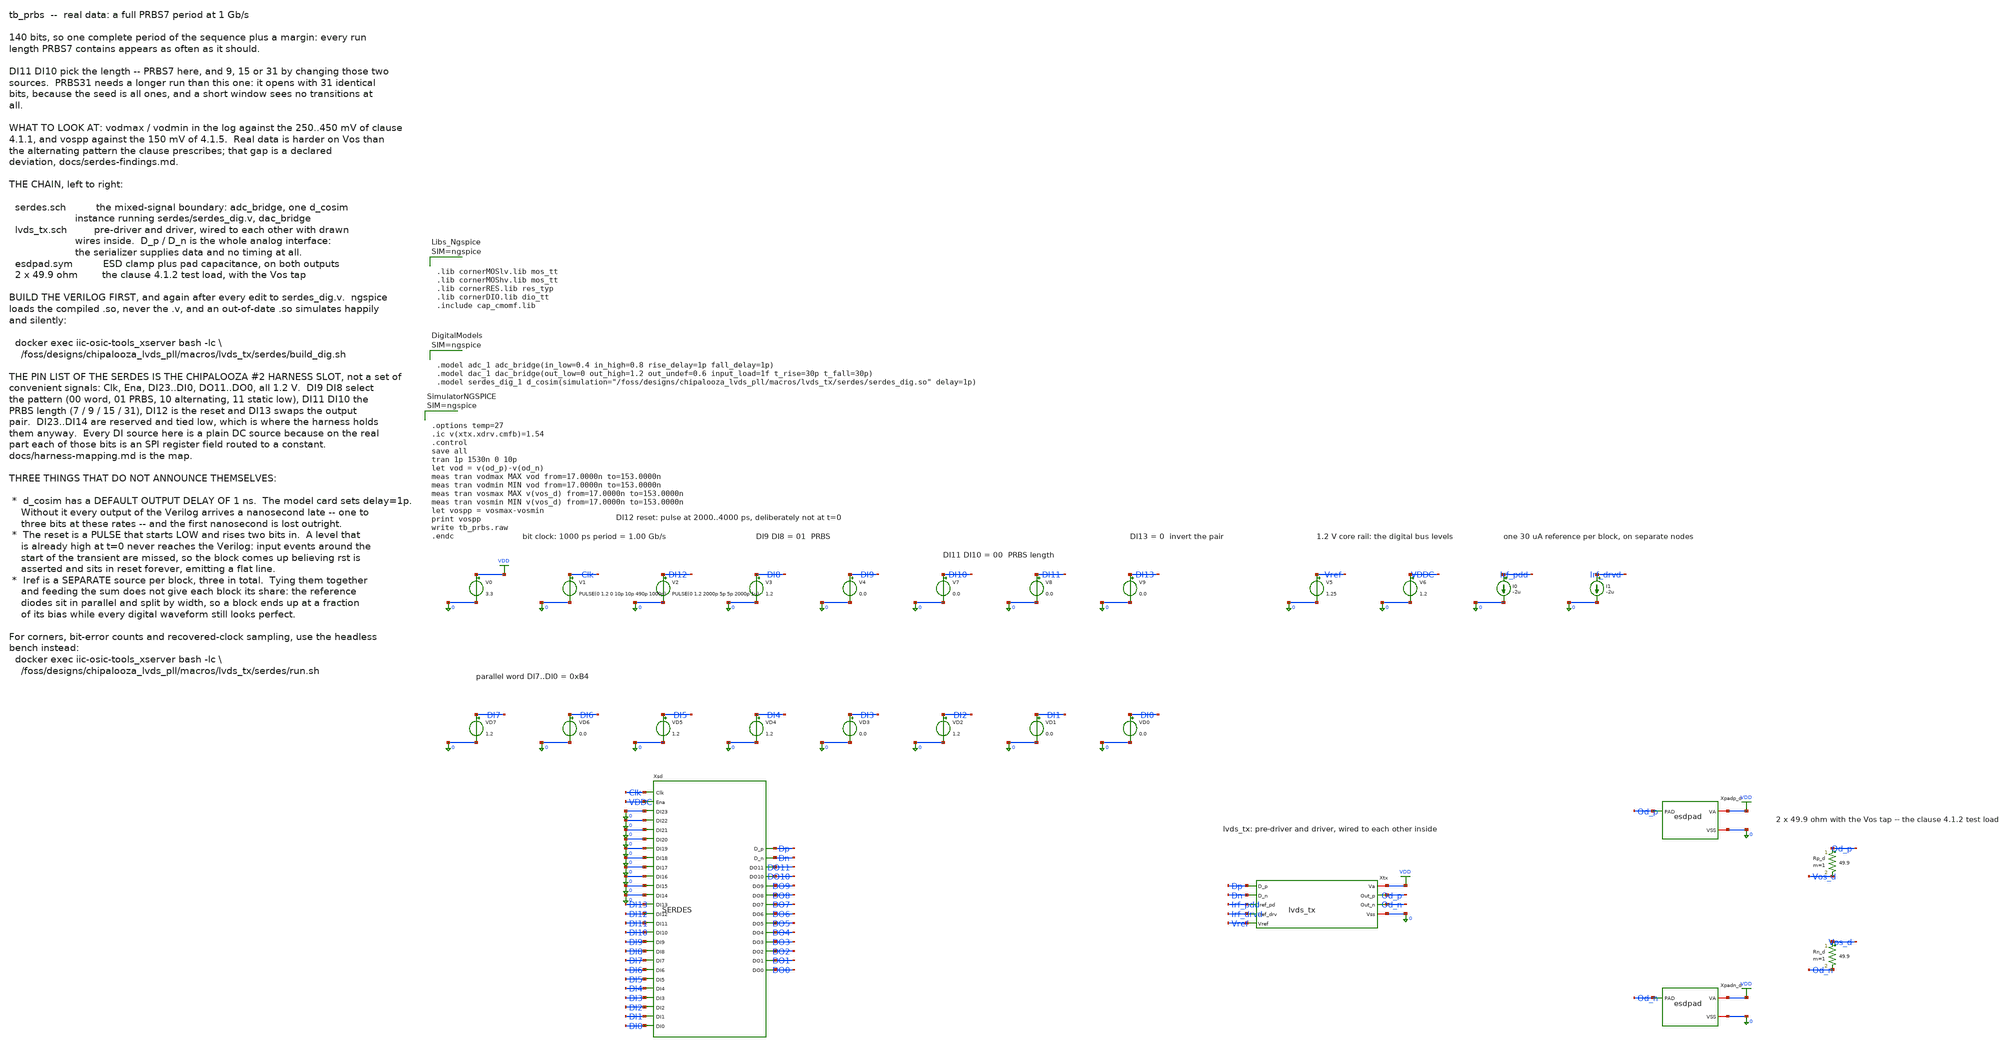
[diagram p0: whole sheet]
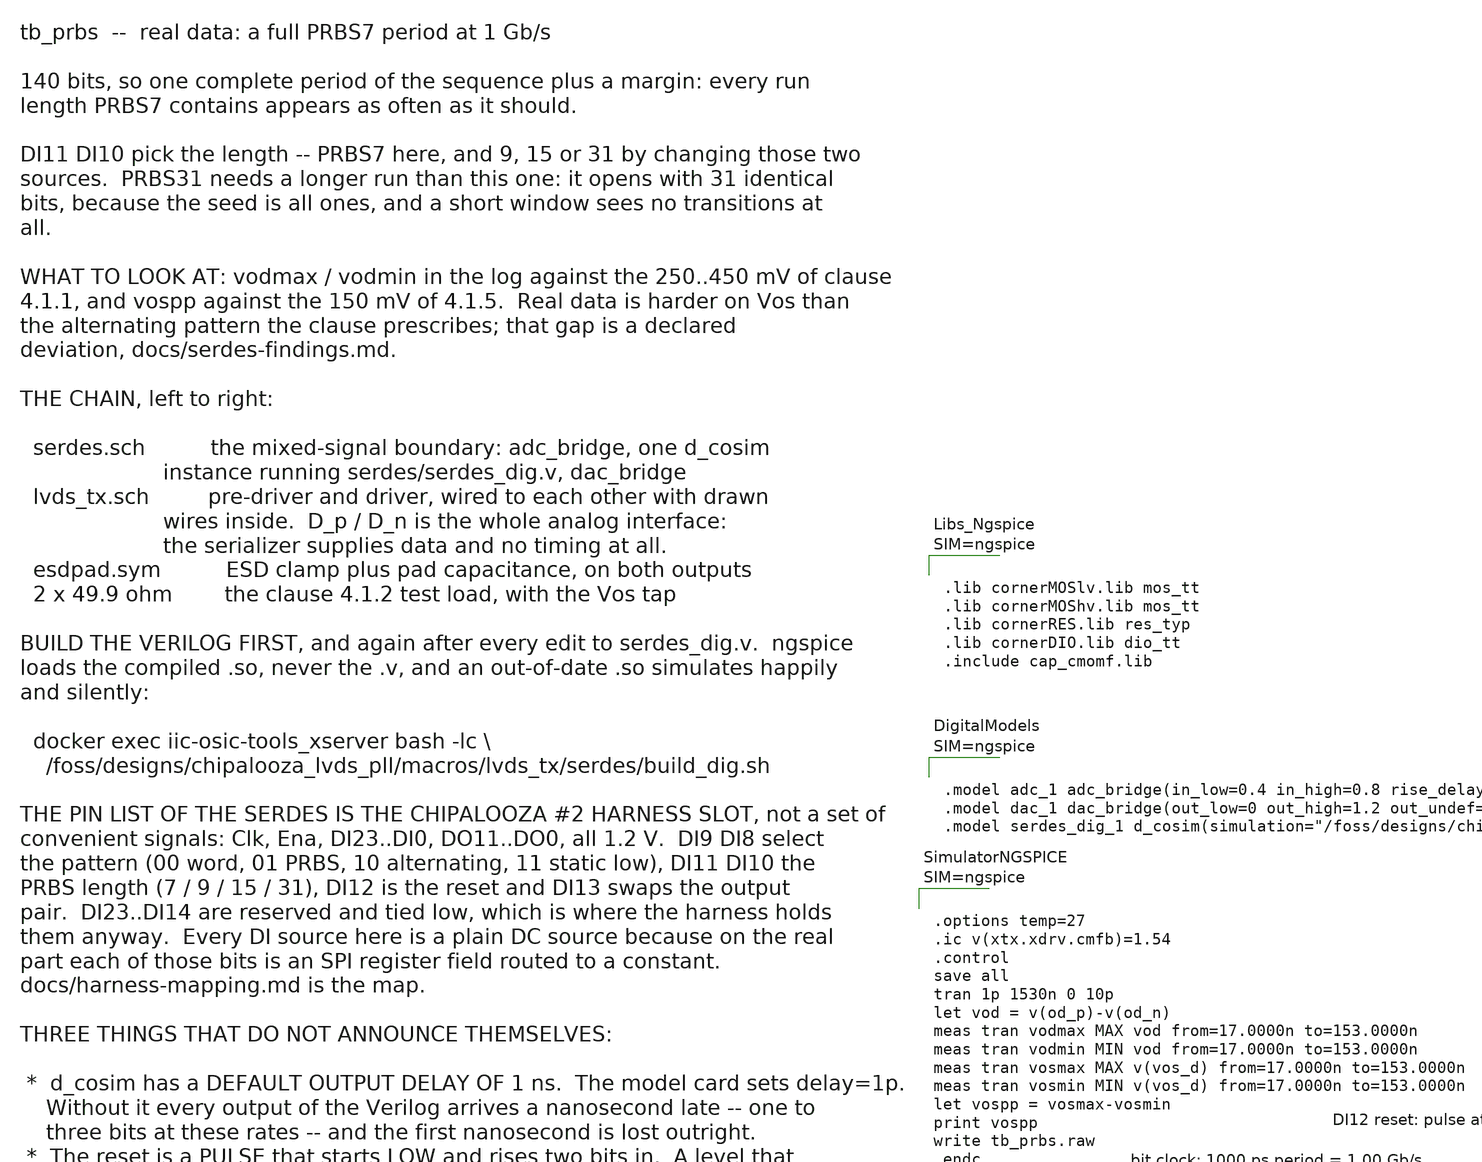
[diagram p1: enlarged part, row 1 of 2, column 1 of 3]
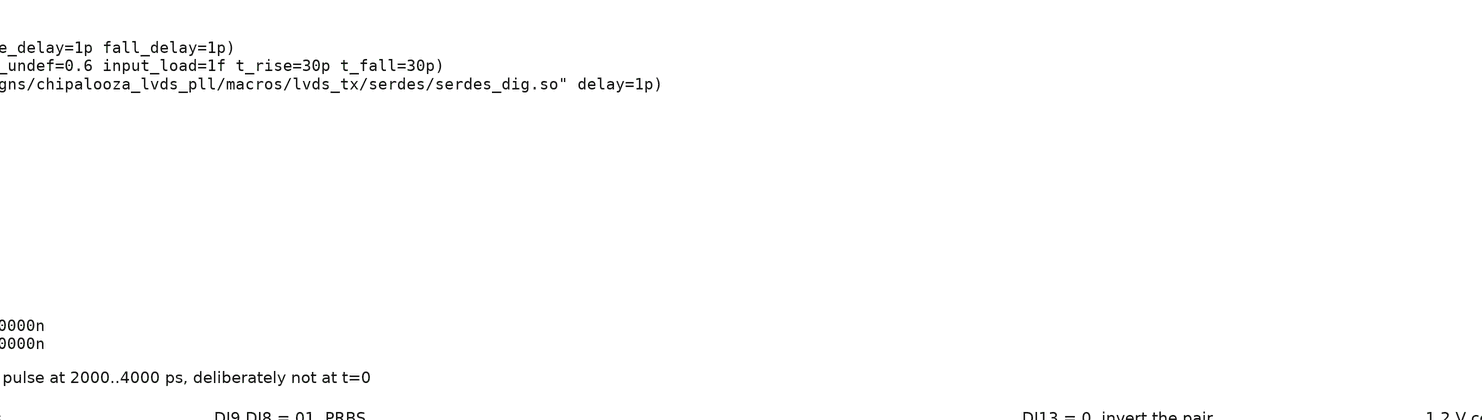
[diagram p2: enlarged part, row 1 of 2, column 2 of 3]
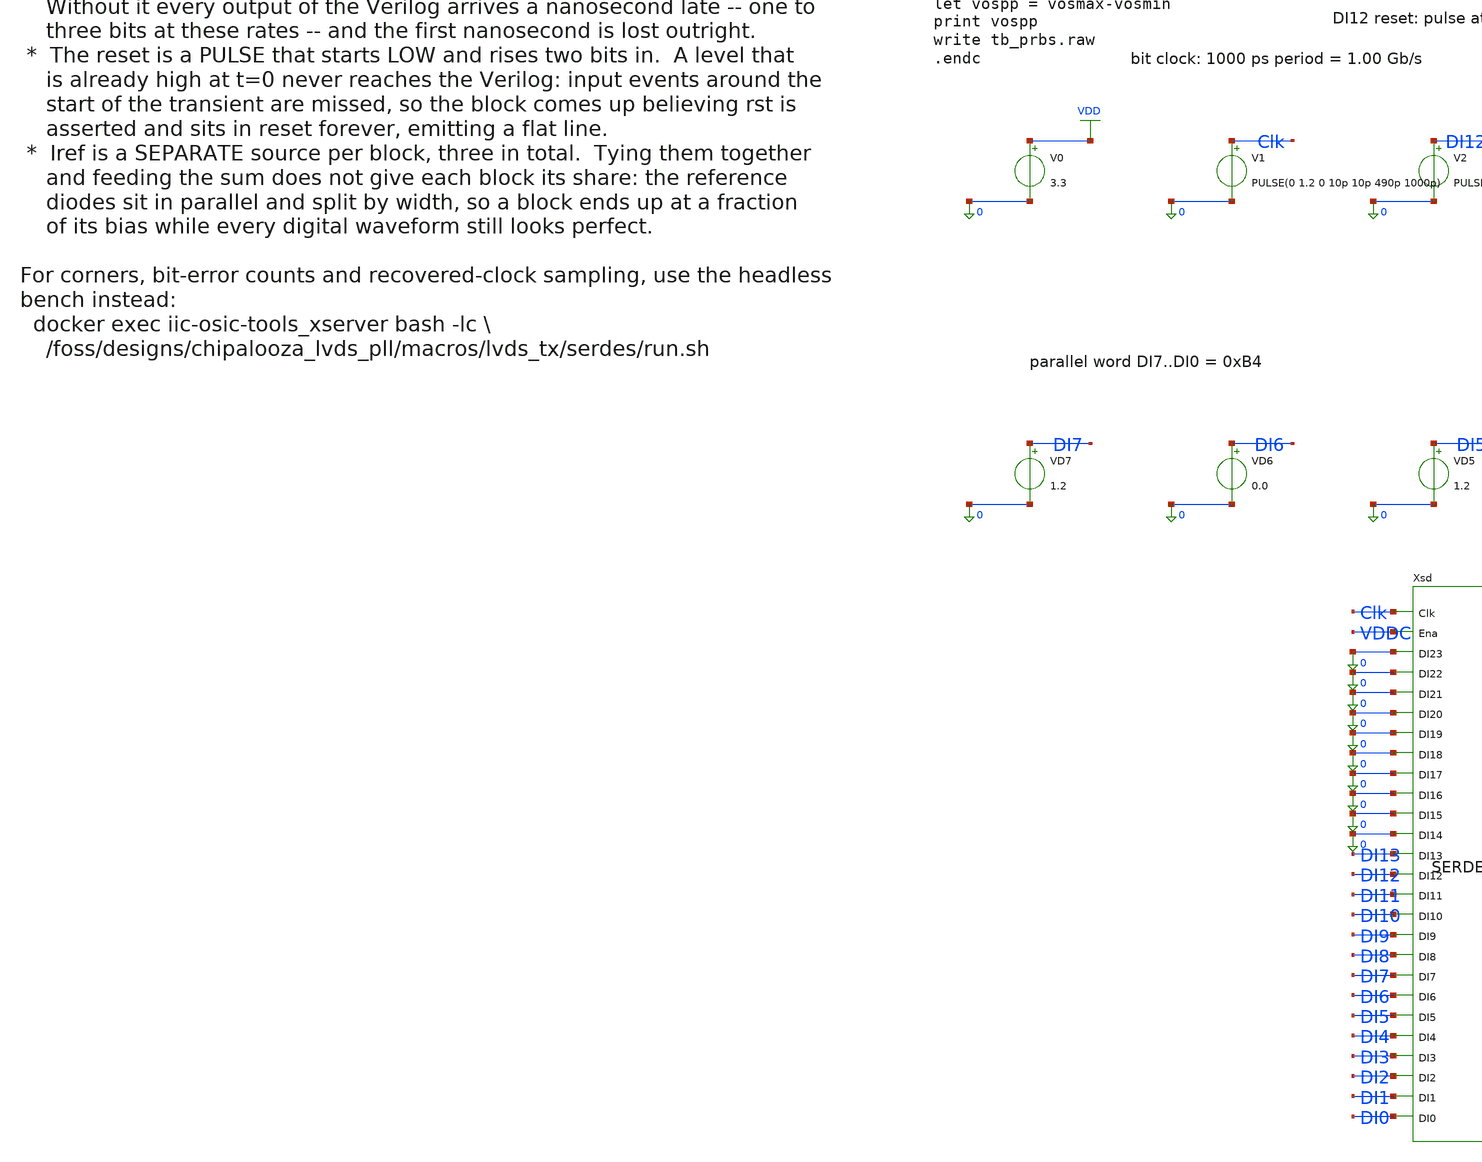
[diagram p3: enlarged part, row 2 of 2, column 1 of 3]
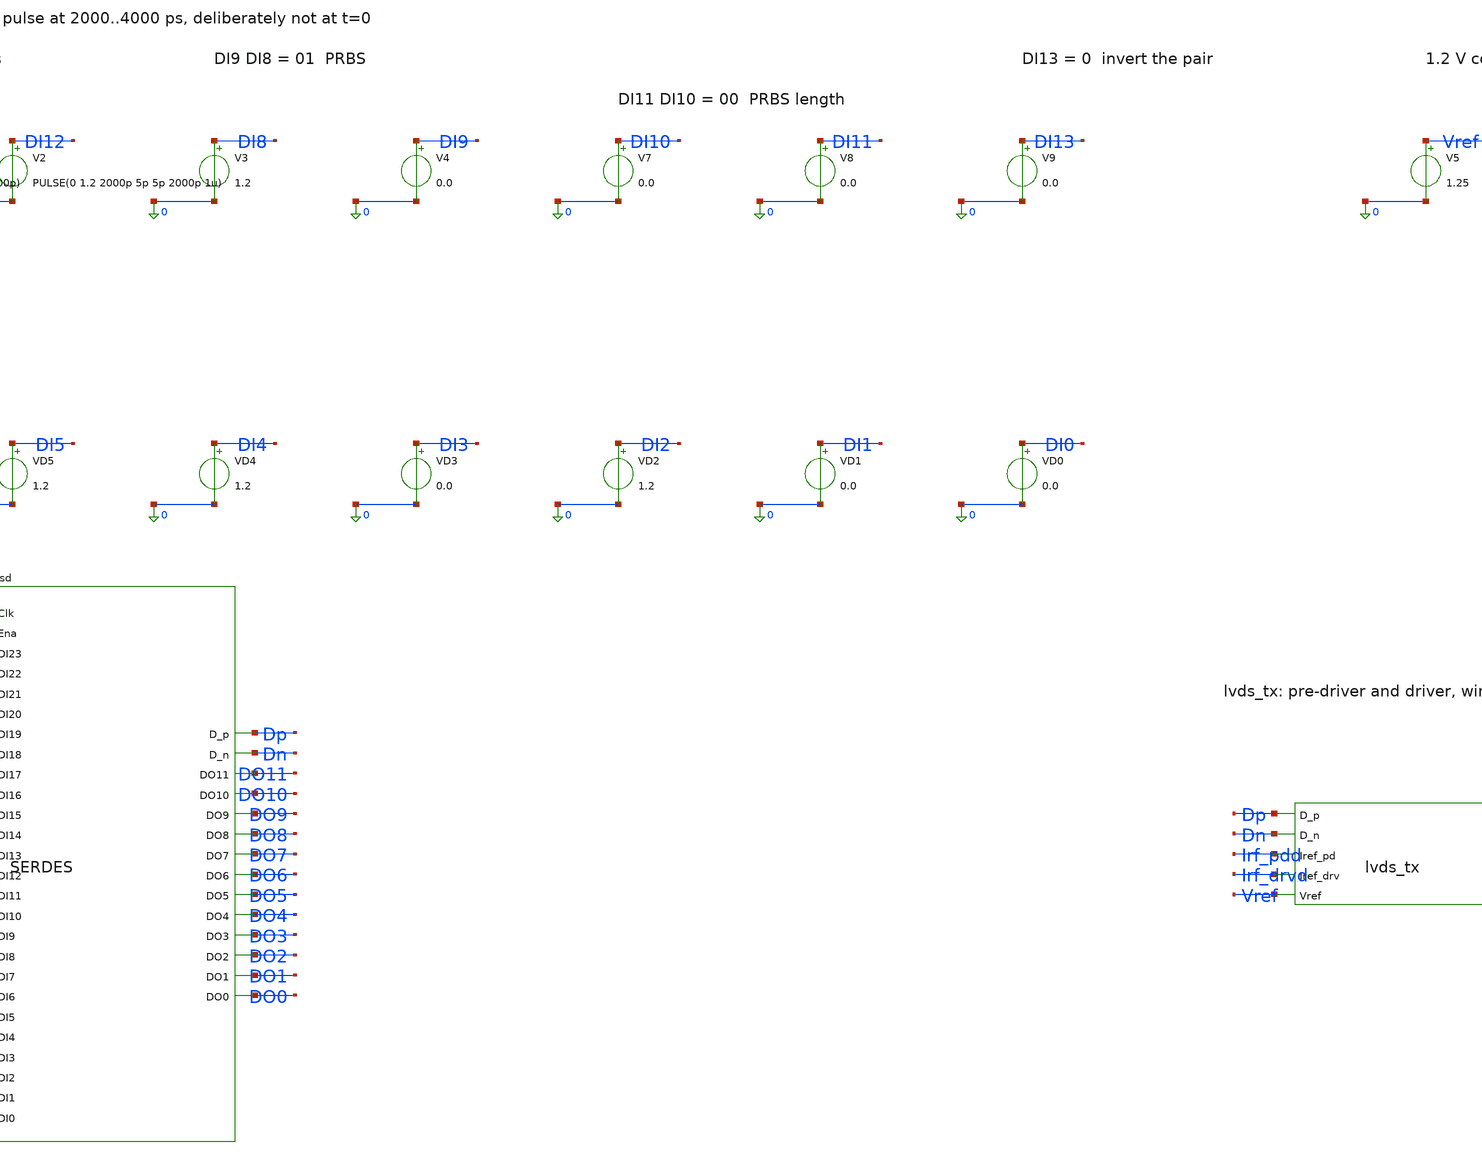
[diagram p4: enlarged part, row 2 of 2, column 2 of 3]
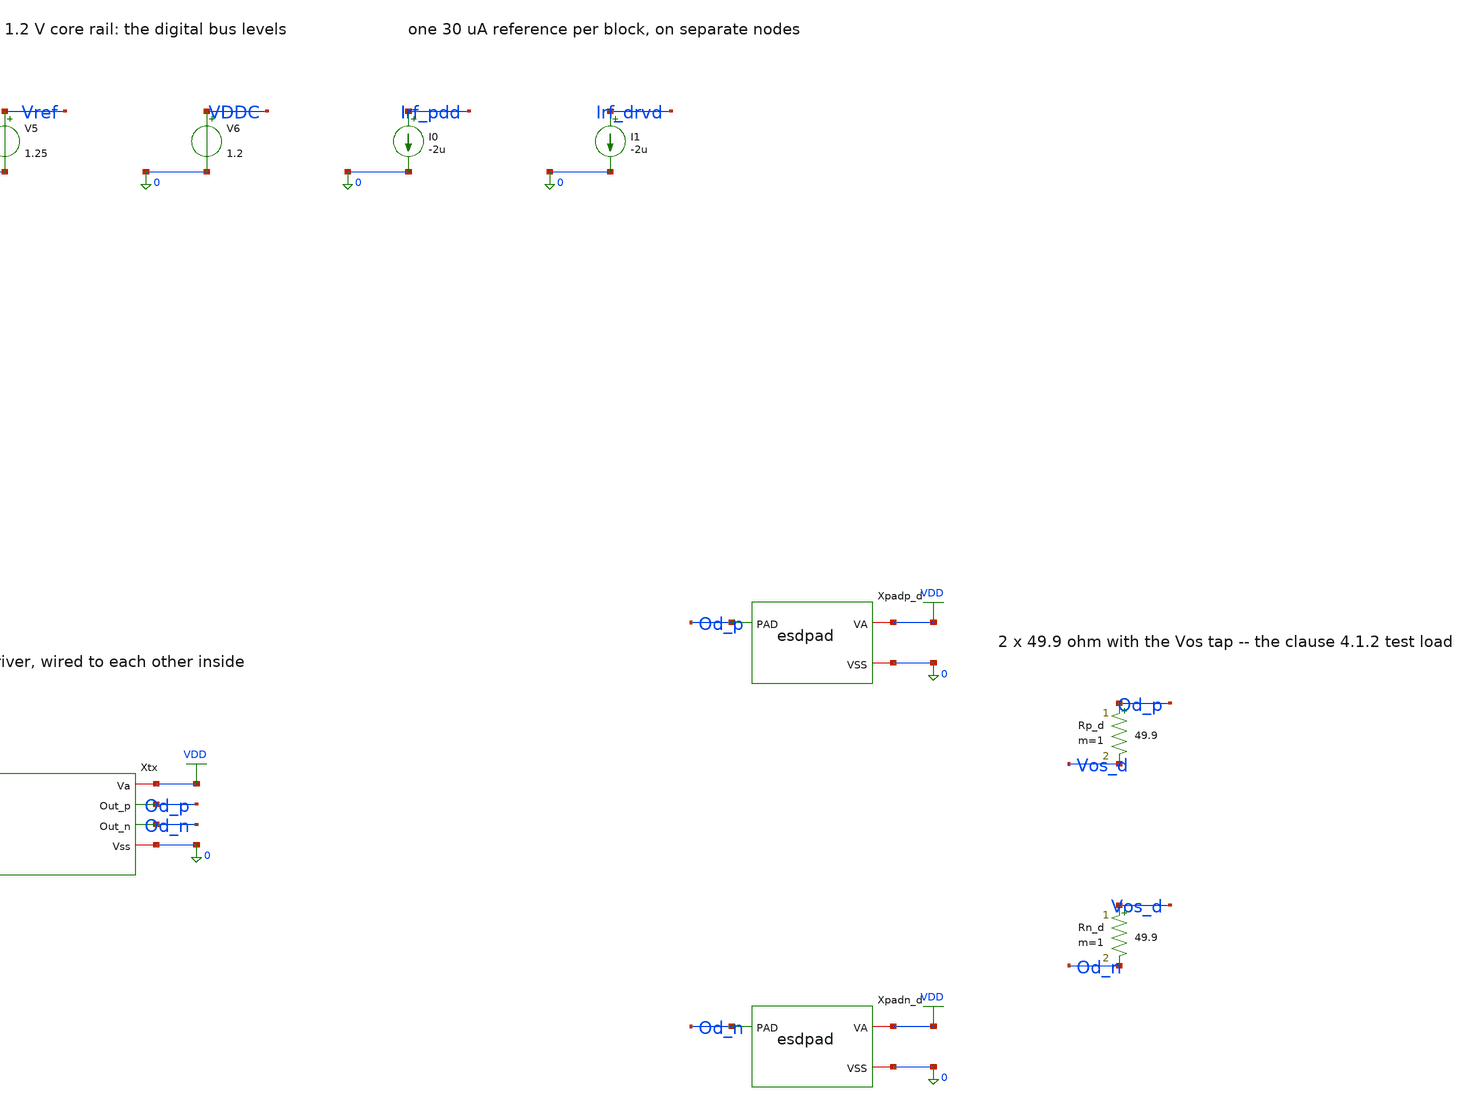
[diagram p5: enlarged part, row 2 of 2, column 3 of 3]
** sch_path: macros/lvds_tx/testbenches/xschem/tb_prbs.sch
**.subckt tb_prbs
V0 VDD 0 3.3
V1 Clk 0 PULSE(0 1.2 0 10p 10p 490p 1000p)
V2 DI12 0 PULSE(0 1.2 2000p 5p 5p 2000p 1u)
V3 DI8 0 1.2
V4 DI9 0 0.0
V7 DI10 0 0.0
V8 DI11 0 0.0
V9 DI13 0 0.0
VD7 DI7 0 1.2
VD6 DI6 0 0.0
VD5 DI5 0 1.2
VD4 DI4 0 1.2
VD3 DI3 0 0.0
VD2 DI2 0 1.2
VD1 DI1 0 0.0
VD0 DI0 0 0.0
V5 Vref 0 1.25
V6 VDDC 0 1.2
I0 Irf_pdd 0 -2u
I1 Irf_drvd 0 -2u
Xsd Clk VDDC 0 0 0 0 0 0 0 0 0 0 DI13 DI12 DI11 DI10 DI9 DI8 DI7 DI6 DI5 DI4 DI3 DI2 DI1 DI0 Dp Dn
+ DO11 DO10 DO9 DO8 DO7 DO6 DO5 DO4 DO3 DO2 DO1 DO0 serdes
Xtx Dp Dn Irf_pdd Irf_drvd Vref VDD Od_p Od_n 0 lvds_tx
Xpadp_d Od_p VDD 0 esdpad
Xpadn_d Od_n VDD 0 esdpad
Rp_d Od_p Vos_d 49.9 m=1
Rn_d Vos_d Od_n 49.9 m=1
**** begin user architecture code



.lib cornerMOSlv.lib mos_tt
.lib cornerMOShv.lib mos_tt
.lib cornerRES.lib res_typ
.lib cornerDIO.lib dio_tt
.include cap_cmomf.lib






.model adc_1 adc_bridge(in_low=0.4 in_high=0.8 rise_delay=1p fall_delay=1p)
.model dac_1 dac_bridge(out_low=0 out_high=1.2 out_undef=0.6 input_load=1f t_rise=30p t_fall=30p)
.model serdes_dig_1
+ d_cosim(simulation="/foss/designs/chipalooza_lvds_pll/macros/lvds_tx/serdes/serdes_dig.so" delay=1p)






.options temp=27
.ic v(xtx.xdrv.cmfb)=1.54
.control
save all
tran 1p 1530n 0 10p
let vod = v(od_p)-v(od_n)
meas tran vodmax MAX vod from=17.0000n to=153.0000n
meas tran vodmin MIN vod from=17.0000n to=153.0000n
meas tran vosmax MAX v(vos_d) from=17.0000n to=153.0000n
meas tran vosmin MIN v(vos_d) from=17.0000n to=153.0000n
let vospp = vosmax-vosmin
print vospp
write tb_prbs.raw
.endc



**** end user architecture code
**.ends

* expanding   symbol:  serdes.sym # of pins=40
** sym_path: macros/lvds_tx/schematic/xschem/serdes.sym
** sch_path: macros/lvds_tx/schematic/xschem/serdes.sch
.subckt serdes Clk Ena DI23 DI22 DI21 DI20 DI19 DI18 DI17 DI16 DI15 DI14 DI13 DI12 DI11 DI10 DI9 DI8
+ DI7 DI6 DI5 DI4 DI3 DI2 DI1 DI0 D_p D_n DO11 DO10 DO9 DO8 DO7 DO6 DO5 DO4 DO3 DO2 DO1 DO0
*.ipin Clk
*.ipin Ena
*.ipin DI23
*.ipin DI22
*.ipin DI21
*.ipin DI20
*.ipin DI19
*.ipin DI18
*.ipin DI17
*.ipin DI16
*.ipin DI15
*.ipin DI14
*.ipin DI13
*.ipin DI12
*.ipin DI11
*.ipin DI10
*.ipin DI9
*.ipin DI8
*.ipin DI7
*.ipin DI6
*.ipin DI5
*.ipin DI4
*.ipin DI3
*.ipin DI2
*.ipin DI1
*.ipin DI0
*.opin D_p
*.opin D_n
*.opin DO11
*.opin DO10
*.opin DO9
*.opin DO8
*.opin DO7
*.opin DO6
*.opin DO5
*.opin DO4
*.opin DO3
*.opin DO2
*.opin DO1
*.opin DO0
A100 [ Clk ] [ dclk ] adc_1
A101 [ Ena ] [ dena ] adc_1
A102 [ DI23 ] [ ddi23 ] adc_1
A103 [ DI22 ] [ ddi22 ] adc_1
A104 [ DI21 ] [ ddi21 ] adc_1
A105 [ DI20 ] [ ddi20 ] adc_1
A106 [ DI19 ] [ ddi19 ] adc_1
A107 [ DI18 ] [ ddi18 ] adc_1
A108 [ DI17 ] [ ddi17 ] adc_1
A109 [ DI16 ] [ ddi16 ] adc_1
A110 [ DI15 ] [ ddi15 ] adc_1
A111 [ DI14 ] [ ddi14 ] adc_1
A112 [ DI13 ] [ ddi13 ] adc_1
A113 [ DI12 ] [ ddi12 ] adc_1
A114 [ DI11 ] [ ddi11 ] adc_1
A115 [ DI10 ] [ ddi10 ] adc_1
A116 [ DI9 ] [ ddi9 ] adc_1
A117 [ DI8 ] [ ddi8 ] adc_1
A118 [ DI7 ] [ ddi7 ] adc_1
A119 [ DI6 ] [ ddi6 ] adc_1
A120 [ DI5 ] [ ddi5 ] adc_1
A121 [ DI4 ] [ ddi4 ] adc_1
A122 [ DI3 ] [ ddi3 ] adc_1
A123 [ DI2 ] [ ddi2 ] adc_1
A124 [ DI1 ] [ ddi1 ] adc_1
A125 [ DI0 ] [ ddi0 ] adc_1
Adig [ dclk dena ddi23 ddi22 ddi21 ddi20 ddi19 ddi18 ddi17 ddi16 ddi15 ddi14 ddi13 ddi12 ddi11 ddi10
+ ddi9 ddi8 ddi7 ddi6 ddi5 ddi4 ddi3 ddi2 ddi1 ddi0 ] [ ddp ddn ddo11 ddo10 ddo9 ddo8 ddo7 ddo6 ddo5 ddo4
+ ddo3 ddo2 ddo1 ddo0 ] serdes_dig_1
A200 [ ddp ] [ D_p ] dac_1
A201 [ ddn ] [ D_n ] dac_1
A202 [ ddo11 ] [ DO11 ] dac_1
A203 [ ddo10 ] [ DO10 ] dac_1
A204 [ ddo9 ] [ DO9 ] dac_1
A205 [ ddo8 ] [ DO8 ] dac_1
A206 [ ddo7 ] [ DO7 ] dac_1
A207 [ ddo6 ] [ DO6 ] dac_1
A208 [ ddo5 ] [ DO5 ] dac_1
A209 [ ddo4 ] [ DO4 ] dac_1
A210 [ ddo3 ] [ DO3 ] dac_1
A211 [ ddo2 ] [ DO2 ] dac_1
A212 [ ddo1 ] [ DO1 ] dac_1
A213 [ ddo0 ] [ DO0 ] dac_1
.ends


* expanding   symbol:  lvds_tx.sym # of pins=9
** sym_path: macros/lvds_tx/schematic/xschem/lvds_tx.sym
** sch_path: macros/lvds_tx/schematic/xschem/lvds_tx.sch
.subckt lvds_tx D_p D_n Iref_pd Iref_drv Vref Va Out_p Out_n Vss
*.ipin D_p
*.ipin D_n
*.ipin Iref_pd
*.ipin Iref_drv
*.ipin Vref
*.iopin Va
*.iopin Vss
*.opin Out_p
*.opin Out_n
Xm_pd Iref_pd Iref_pd_30u Va Vss iref_x15
Xm_drv Iref_drv Iref_drv_30u Va Vss iref_x15
Xpd D_p D_n Iref_pd_30u In_p In_n Va Vss predriver
Xdrv Va Out_p In_p In_n Iref_drv_30u Vref Out_n Vss Driver
.ends


* expanding   symbol:  esdpad.sym # of pins=3
** sym_path: macros/lvds_tx/schematic/xschem/esdpad.sym
** sch_path: macros/lvds_tx/schematic/xschem/esdpad.sch
.subckt esdpad PAD VA VSS
*.iopin PAD
*.iopin VA
*.iopin VSS
XDdvdd VA PAD VSS diodevdd_4kv m=1
XDdvss VA PAD VSS diodevss_4kv m=1
Cpad PAD VSS 90f m=1
.ends


* expanding   symbol:  iref_x15.sym # of pins=4
** sym_path: macros/iref_x15/schematic/xschem/iref_x15.sym
** sch_path: macros/iref_x15/schematic/xschem/iref_x15.sch
.subckt iref_x15 IREF_IN IREF_OUT Va Vss
*.ipin IREF_IN
*.opin IREF_OUT
*.iopin Va
*.iopin Vss
XMn1 IREF_IN IREF_IN Vss Vss sg13_hv_nmos w=3.2u l=2u ng=1 m=1 mm_ok=1
XMn2 CASC IREF_IN Vss Vss sg13_hv_nmos w=48u l=2u ng=6 m=1 mm_ok=1
XMp1 CASC CASC Va Va sg13_hv_pmos w=48u l=2u ng=6 m=1 mm_ok=1
XMp2 IREF_OUT CASC Va Va sg13_hv_pmos w=48u l=2u ng=6 m=1 mm_ok=1
.ends


* expanding   symbol:  predriver.sym # of pins=7
** sym_path: macros/lvds_tx/schematic/xschem/predriver.sym
** sch_path: macros/lvds_tx/schematic/xschem/predriver.sch
.subckt predriver D_p D_n Iref In_p In_n Va Vss
*.iopin Va
*.iopin Vss
*.ipin Iref
*.ipin D_p
*.ipin D_n
*.opin In_p
*.opin In_n
Xkpm D_p D_n Iref net1 Va Vss predriver_comp
XMref Iref Iref Vss Vss sg13_hv_nmos w=8u l=0.5u ng=1 m=1 mm_ok=1
Xknm D_n D_p Iref net2 Va Vss predriver_comp
Xstm net1 net2 In_p In_n Va Vss predriver_stage
.ends


* expanding   symbol:  Driver.sym # of pins=8
** sym_path: macros/lvds_tx/schematic/xschem/Driver.sym
** sch_path: macros/lvds_tx/schematic/xschem/Driver.sch
.subckt Driver Va Out_p In_p In_n Iref Vref Out_n Vss
*.iopin Va
*.iopin Vss
*.opin Out_p
*.opin Out_n
*.ipin In_p
*.ipin In_n
*.ipin Iref
*.ipin Vref
XCtn1 Va tail_n Va Va sg13_hv_pmos w=11.8u l=5.25u ng=2 m=1 mm_ok=1
XCtn2 Va tail_n Va Va sg13_hv_pmos w=5.7u l=5.8u ng=2 m=1 mm_ok=1
XM2 tail_p cmfb Va Va sg13_hv_pmos w=97.2u l=0.5u ng=20 m=1 mm_ok=1
XM5 Out_p In_p tail_p Va sg13_hv_pmos w=80u l=0.4u ng=16 m=1 mm_ok=1
XM4 Out_n In_n tail_p Va sg13_hv_pmos w=80u l=0.4u ng=16 m=1 mm_ok=1
XM1 Out_p In_p tail_n Vss sg13_hv_nmos w=30u l=0.45u ng=15 m=1 mm_ok=1
XM3 Out_n In_n tail_n Vss sg13_hv_nmos w=30u l=0.45u ng=15 m=1 mm_ok=1
XM6 tail_n Iref Vss Vss sg13_hv_nmos w=49.6u l=0.5u ng=31 m=2 mm_ok=1
XM9 Iref Iref Vss Vss sg13_hv_nmos w=0.8u l=0.5u ng=1 m=1 mm_ok=1
XM13 pd pd Va Va sg13_hv_pmos w=5u l=1u ng=1 m=1 mm_ok=1
XM14 cmfb pd Va Va sg13_hv_pmos w=5u l=1u ng=1 m=1 mm_ok=1
XM11 pd cm otail Vss sg13_hv_nmos w=40u l=1u ng=16 m=1 mm_ok=1
XM12 cmfb Vref otail Vss sg13_hv_nmos w=40u l=1u ng=16 m=1 mm_ok=1
XM10 otail Iref Vss Vss sg13_hv_nmos w=0.8u l=0.5u ng=1 m=1 mm_ok=1
XCc Va cc_g Va Va sg13_hv_pmos w=50u l=5u ng=10 m=1 mm_ok=1
XRc cmfb cc_g Vss rppd w=1u l=6u m=1 b=0 mm_ok=1
XRp Out_p cm Vss rhigh w=1u l=7.35u m=1 b=0 mm_ok=1
XRn Out_n cm Vss rhigh w=1u l=7.35u m=1 b=0 mm_ok=1
XCxp Out_p In_n cap_cmomf w=5.913u l=5.913u mmin=1 mmax=4 subblock=0 rfmodel=0 subscale=1 m=1
+ mm_ok=1
XCxn Out_n In_p cap_cmomf w=5.913u l=5.913u mmin=1 mmax=4 subblock=0 rfmodel=0 subscale=1 m=1
+ mm_ok=1
XCop Vss Out_p Vss Vss sg13_hv_nmos w=10u l=5u ng=1 m=2 mm_ok=1
XCon Vss Out_n Vss Vss sg13_hv_nmos w=10u l=5u ng=1 m=2 mm_ok=1
.ends


* expanding   symbol:  predriver_comp.sym # of pins=6
** sym_path: macros/lvds_tx/schematic/xschem/predriver_comp.sym
** sch_path: macros/lvds_tx/schematic/xschem/predriver_comp.sch
.subckt predriver_comp Gin Din Iref Out Va Vss
*.iopin Va
*.iopin Vss
*.opin Out
*.ipin Din
*.ipin Gin
*.ipin Iref
XMld net1 net1 Va Va sg13_hv_pmos w=12u l=0.4u ng=4 m=1 mm_ok=1
XMlo Out net1 Va Va sg13_hv_pmos w=12u l=0.4u ng=4 m=1 mm_ok=1
XMid net1 Din net2 Vss sg13_hv_nmos w=24u l=0.45u ng=6 m=1 mm_ok=1
XMio Out Gin net2 Vss sg13_hv_nmos w=24u l=0.45u ng=6 m=1 mm_ok=1
XMt net2 Iref Vss Vss sg13_hv_nmos w=17.52u l=0.45u ng=6 m=2 mm_ok=1
.ends


* expanding   symbol:  predriver_stage.sym # of pins=6
** sym_path: macros/lvds_tx/schematic/xschem/predriver_stage.sym
** sch_path: macros/lvds_tx/schematic/xschem/predriver_stage.sch
.subckt predriver_stage In_p In_n Out_p Out_n Va Vss
*.ipin In_p
*.opin Out_p
*.ipin In_n
*.opin Out_n
*.iopin Va
*.iopin Vss
XMpp0 net1 In_p Va Va sg13_hv_pmos w=2.64u l=0.4u ng=1 m=1 mm_ok=1
XMnp0 net1 In_p Vss Vss sg13_hv_nmos w=1.6u l=0.45u ng=1 m=1 mm_ok=1
XMpp1 net2 net1 Va Va sg13_hv_pmos w=12.52u l=0.4u ng=4 m=1 mm_ok=1
XMnp1 net2 net1 Vss Vss sg13_hv_nmos w=5u l=0.45u ng=4 m=1 mm_ok=1
XMpp2 Out_p net2 Va Va sg13_hv_pmos w=40u l=0.4u ng=10 m=1 mm_ok=1
XMnp2 Out_p net2 Vss Vss sg13_hv_nmos w=16u l=0.45u ng=10 m=1 mm_ok=1
XMpn0 net3 In_n Va Va sg13_hv_pmos w=2.64u l=0.4u ng=1 m=1 mm_ok=1
XMnn0 net3 In_n Vss Vss sg13_hv_nmos w=1.6u l=0.45u ng=1 m=1 mm_ok=1
XMpn1 net4 net3 Va Va sg13_hv_pmos w=12.52u l=0.4u ng=4 m=1 mm_ok=1
XMnn1 net4 net3 Vss Vss sg13_hv_nmos w=5u l=0.45u ng=4 m=1 mm_ok=1
XMpn2 Out_n net4 Va Va sg13_hv_pmos w=40u l=0.4u ng=10 m=1 mm_ok=1
XMnn2 Out_n net4 Vss Vss sg13_hv_nmos w=16u l=0.45u ng=10 m=1 mm_ok=1
XMpxp net4 net2 Va Va sg13_hv_pmos w=4.38u l=0.4u ng=1 m=1 mm_ok=1
XMnxp net4 net2 Vss Vss sg13_hv_nmos w=1.75u l=0.45u ng=1 m=1 mm_ok=1
XMpxn net2 net4 Va Va sg13_hv_pmos w=4.38u l=0.4u ng=1 m=1 mm_ok=1
XMnxn net2 net4 Vss Vss sg13_hv_nmos w=1.75u l=0.45u ng=1 m=1 mm_ok=1
.ends

.GLOBAL VDD
.end
